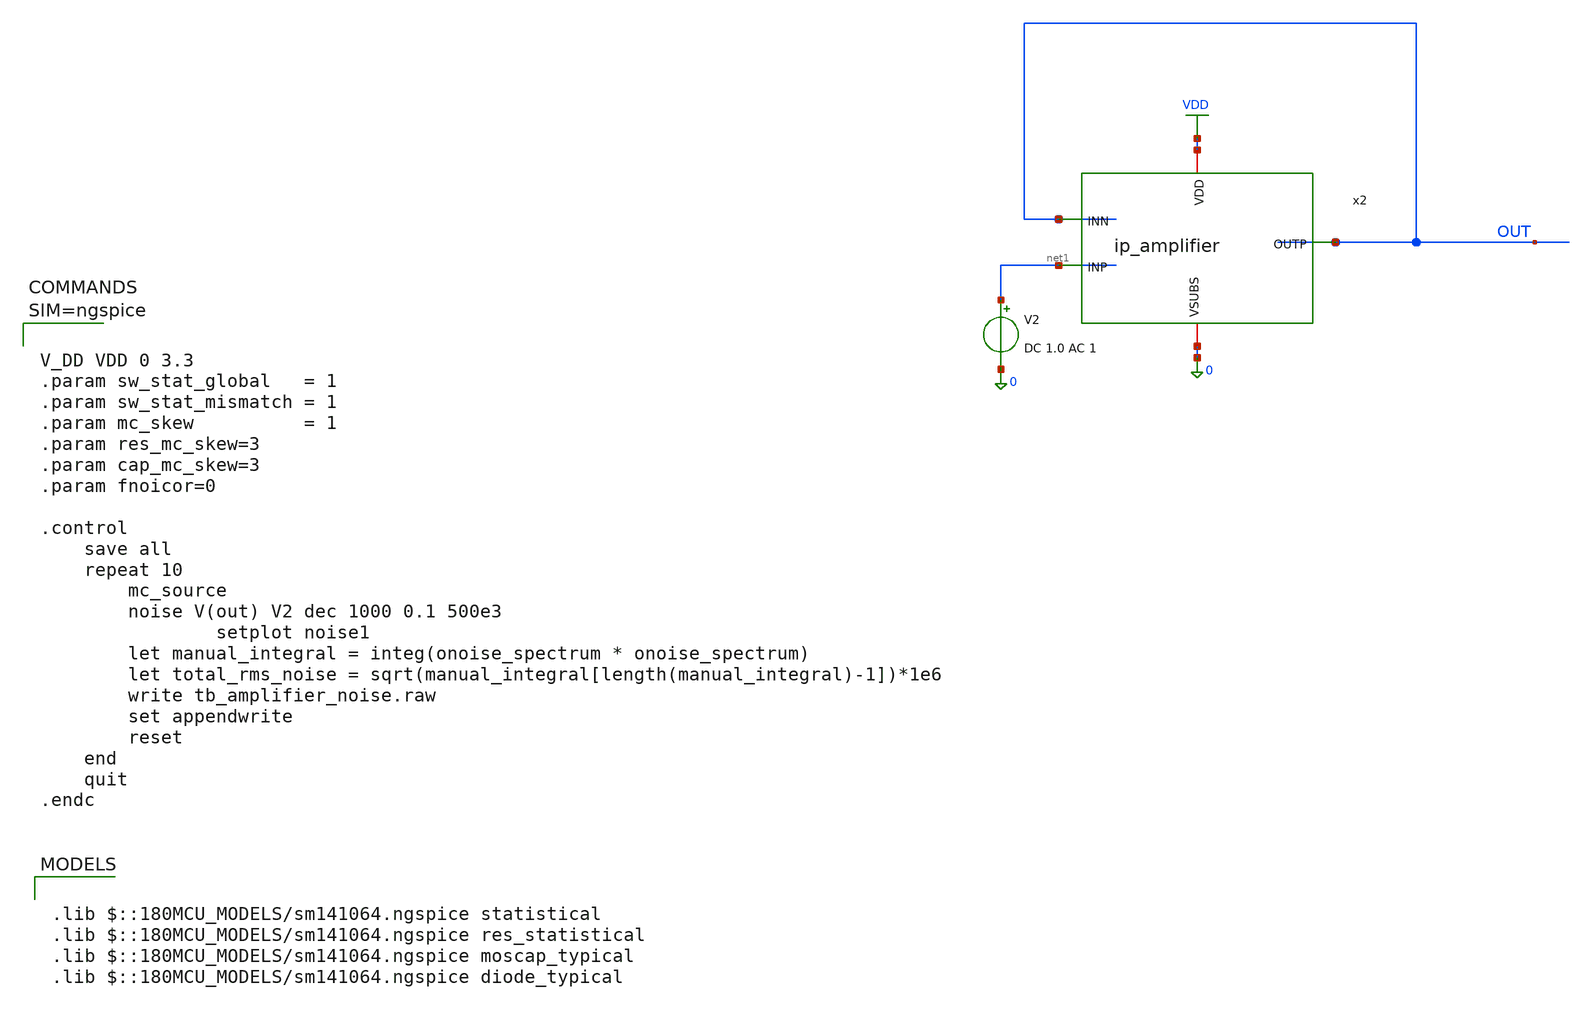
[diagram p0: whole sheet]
** sch_path: xschem/tb_amplifier_noise.sch
**.subckt tb_amplifier_noise
V2 net1 0 DC 1.0 AC 1
x2 VDD OUT net1 OUT 0 ip_amplifier
**** begin user architecture code

.lib $::180MCU_MODELS/sm141064.ngspice statistical
.lib $::180MCU_MODELS/sm141064.ngspice res_statistical
.lib $::180MCU_MODELS/sm141064.ngspice moscap_typical
.lib $::180MCU_MODELS/sm141064.ngspice diode_typical




V_DD VDD 0 3.3
.param sw_stat_global   = 1
.param sw_stat_mismatch = 1
.param mc_skew          = 1
.param res_mc_skew=3
.param cap_mc_skew=3
.param fnoicor=0

.control
	save all
	repeat 10
		mc_source
		noise V(out) V2 dec 1000 0.1 500e3
                setplot noise1
		let manual_integral = integ(onoise_spectrum * onoise_spectrum)
		let total_rms_noise = sqrt(manual_integral[length(manual_integral)-1])*1e6
		write tb_amplifier_noise.raw
		set appendwrite
		reset
	end
	quit
.endc



**** end user architecture code
**.ends
.GLOBAL VDD
.end
